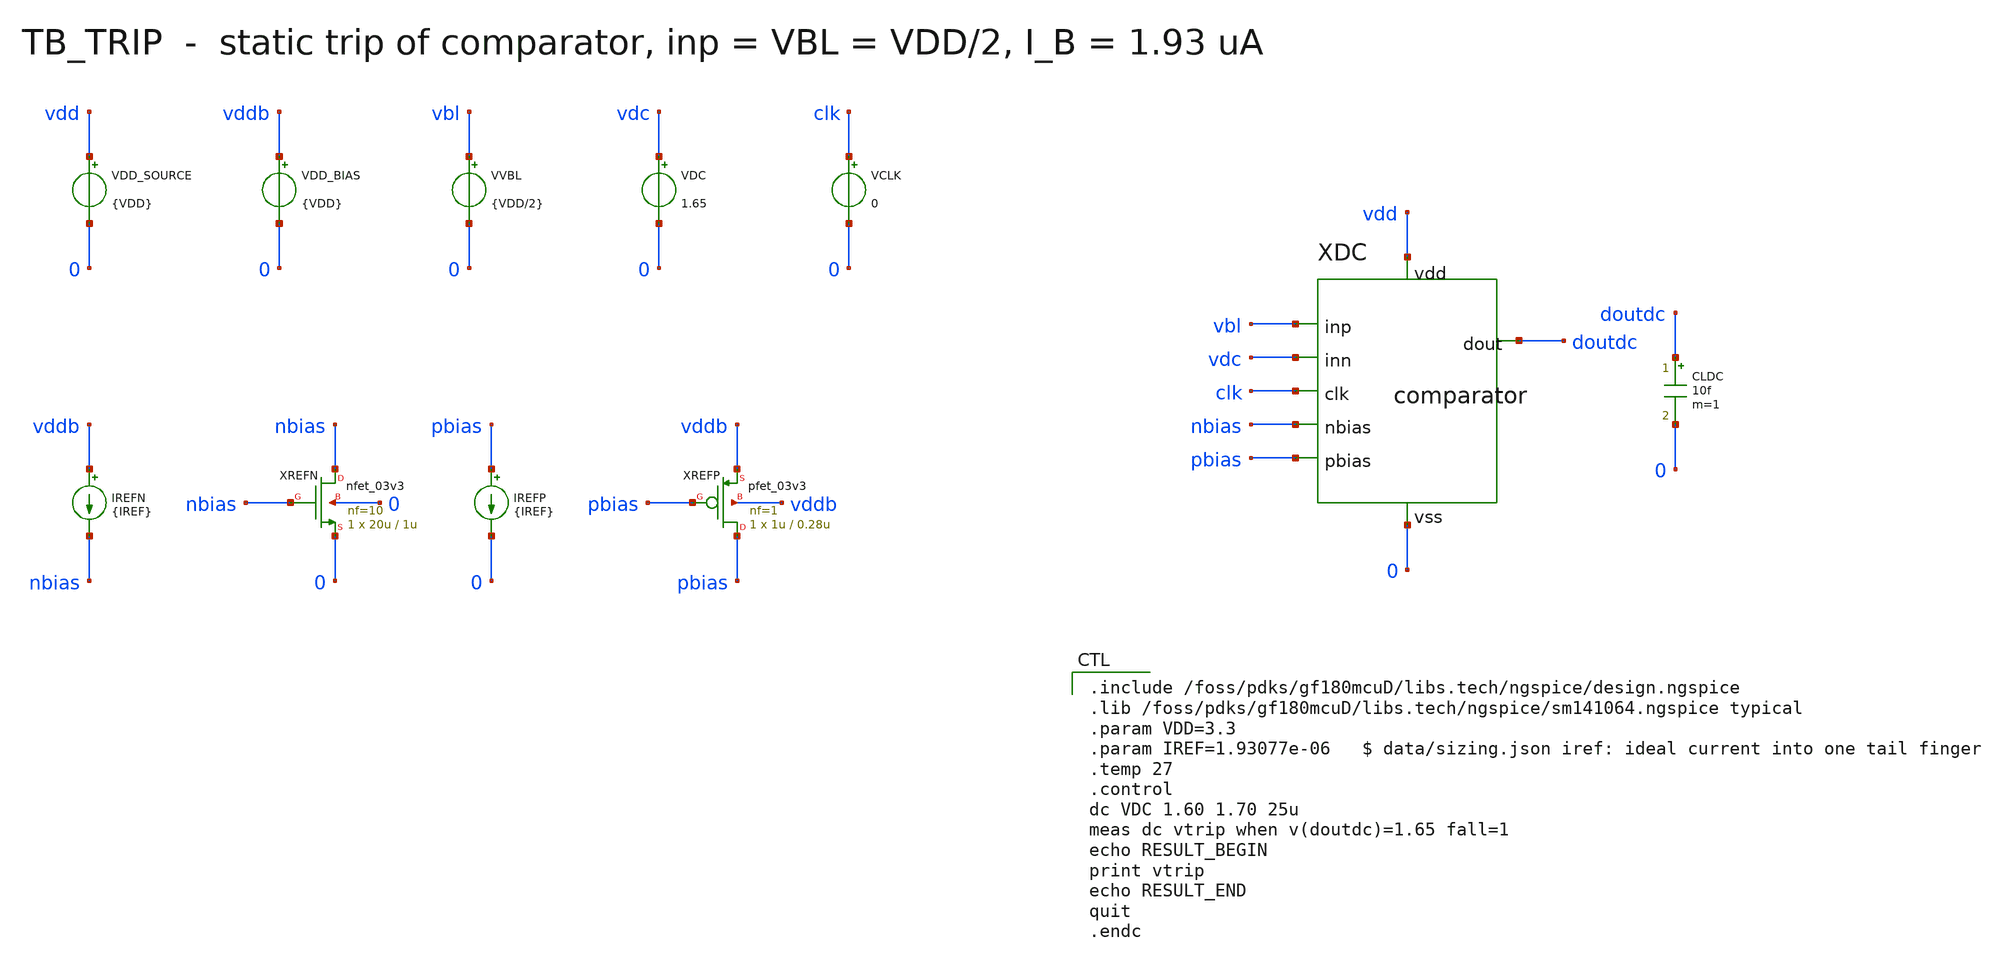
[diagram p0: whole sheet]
** sch_path: mixed_signal/comparator/tb_trip.sch
**.subckt tb_trip
VDD_SOURCE vdd 0 {VDD}
VDD_BIAS vddb 0 {VDD}
VVBL vbl 0 {VDD/2}
VDC vdc 0 1.65
VCLK clk 0 0
IREFN vddb nbias {IREF}
XREFN nbias nbias 0 0 nfet_03v3 L=1u W=20u nf=10 ad='int((nf+1)/2) * W/nf * 0.18u' as='int((nf+2)/2) * W/nf * 0.18u'
+ pd='2*int((nf+1)/2) * (W/nf + 0.18u)' ps='2*int((nf+2)/2) * (W/nf + 0.18u)' nrd='0.18u / W' nrs='0.18u / W'
+ sa=0 sb=0 sd=0 m=1
IREFP pbias 0 {IREF}
XREFP pbias pbias vddb vddb pfet_03v3 L=0.28u W=1u nf=1 ad='int((nf+1)/2) * W/nf * 0.18u' as='int((nf+2)/2) * W/nf * 0.18u'
+ pd='2*int((nf+1)/2) * (W/nf + 0.18u)' ps='2*int((nf+2)/2) * (W/nf + 0.18u)' nrd='0.18u / W' nrs='0.18u / W'
+ sa=0 sb=0 sd=0 m=1
XDC vbl vdc doutdc clk vdd 0 nbias pbias comparator
CLDC doutdc 0 10f m=1
**** begin user architecture code

.include /foss/pdks/gf180mcuD/libs.tech/ngspice/design.ngspice
.lib /foss/pdks/gf180mcuD/libs.tech/ngspice/sm141064.ngspice typical
.param VDD=3.3
.param IREF=1.93077e-06   $ data/sizing.json iref: ideal current into one tail finger
.temp 27
.control
dc VDC 1.60 1.70 25u
meas dc vtrip when v(doutdc)=1.65 fall=1
echo RESULT_BEGIN
print vtrip
echo RESULT_END
quit
.endc

**** end user architecture code
**.ends

* expanding   symbol:  comparator.sym # of pins=8
** sym_path: mixed_signal/comparator/comparator.sym
** sch_path: mixed_signal/comparator/comparator.sch
.subckt comparator inp inn dout clk vdd vss nbias pbias
*.iopin vdd
*.iopin vss
*.ipin pbias
*.ipin inp
*.ipin inn
*.opin dout
*.ipin clk
*.ipin nbias
XTAIL tail pbias vdd vdd pfet_03v3 L=0.28u W=11u nf=11 ad='int((nf+1)/2) * W/nf * 0.18u' as='int((nf+2)/2) * W/nf * 0.18u'
+ pd='2*int((nf+1)/2) * (W/nf + 0.18u)' ps='2*int((nf+2)/2) * (W/nf + 0.18u)' nrd='0.18u / W' nrs='0.18u / W'
+ sa=0 sb=0 sd=0 m=1
XINP left inp tail vdd pfet_03v3 L=0.32u W=12u nf=12 ad='int((nf+1)/2) * W/nf * 0.18u' as='int((nf+2)/2) * W/nf * 0.18u'
+ pd='2*int((nf+1)/2) * (W/nf + 0.18u)' ps='2*int((nf+2)/2) * (W/nf + 0.18u)' nrd='0.18u / W' nrs='0.18u / W'
+ sa=0 sb=0 sd=0 m=1
XINN outa inn tail vdd pfet_03v3 L=0.32u W=12u nf=12 ad='int((nf+1)/2) * W/nf * 0.18u' as='int((nf+2)/2) * W/nf * 0.18u'
+ pd='2*int((nf+1)/2) * (W/nf + 0.18u)' ps='2*int((nf+2)/2) * (W/nf + 0.18u)' nrd='0.18u / W' nrs='0.18u / W'
+ sa=0 sb=0 sd=0 m=1
XLOADD left left vss vss nfet_03v3 L=0.36u W=0.5u nf=1 ad='int((nf+1)/2) * W/nf * 0.18u' as='int((nf+2)/2) * W/nf * 0.18u'
+ pd='2*int((nf+1)/2) * (W/nf + 0.18u)' ps='2*int((nf+2)/2) * (W/nf + 0.18u)' nrd='0.18u / W' nrs='0.18u / W'
+ sa=0 sb=0 sd=0 m=1
XLOADM outa left vss vss nfet_03v3 L=0.36u W=0.5u nf=1 ad='int((nf+1)/2) * W/nf * 0.18u' as='int((nf+2)/2) * W/nf * 0.18u'
+ pd='2*int((nf+1)/2) * (W/nf + 0.18u)' ps='2*int((nf+2)/2) * (W/nf + 0.18u)' nrd='0.18u / W' nrs='0.18u / W'
+ sa=0 sb=0 sd=0 m=1
XBST bst pbias vdd vdd pfet_03v3 L=0.28u W=5u nf=5 ad='int((nf+1)/2) * W/nf * 0.18u' as='int((nf+2)/2) * W/nf * 0.18u'
+ pd='2*int((nf+1)/2) * (W/nf + 0.18u)' ps='2*int((nf+2)/2) * (W/nf + 0.18u)' nrd='0.18u / W' nrs='0.18u / W'
+ sa=0 sb=0 sd=0 m=1
XBUF2 outb outa bst vdd pfet_03v3 L=0.36u W=1u nf=1 ad='int((nf+1)/2) * W/nf * 0.18u' as='int((nf+2)/2) * W/nf * 0.18u'
+ pd='2*int((nf+1)/2) * (W/nf + 0.18u)' ps='2*int((nf+2)/2) * (W/nf + 0.18u)' nrd='0.18u / W' nrs='0.18u / W'
+ sa=0 sb=0 sd=0 m=1
XBUF1 outb outa vss vss nfet_03v3 L=0.36u W=0.5u nf=1 ad='int((nf+1)/2) * W/nf * 0.18u' as='int((nf+2)/2) * W/nf * 0.18u'
+ pd='2*int((nf+1)/2) * (W/nf + 0.18u)' ps='2*int((nf+2)/2) * (W/nf + 0.18u)' nrd='0.18u / W' nrs='0.18u / W'
+ sa=0 sb=0 sd=0 m=1
XBUF4 dout outb vdd vdd pfet_03v3 L=0.36u W=1u nf=1 ad='int((nf+1)/2) * W/nf * 0.18u' as='int((nf+2)/2) * W/nf * 0.18u'
+ pd='2*int((nf+1)/2) * (W/nf + 0.18u)' ps='2*int((nf+2)/2) * (W/nf + 0.18u)' nrd='0.18u / W' nrs='0.18u / W'
+ sa=0 sb=0 sd=0 m=1
XBUF3 dout outb vss vss nfet_03v3 L=0.36u W=0.5u nf=1 ad='int((nf+1)/2) * W/nf * 0.18u' as='int((nf+2)/2) * W/nf * 0.18u'
+ pd='2*int((nf+1)/2) * (W/nf + 0.18u)' ps='2*int((nf+2)/2) * (W/nf + 0.18u)' nrd='0.18u / W' nrs='0.18u / W'
+ sa=0 sb=0 sd=0 m=1
.ends

.end
